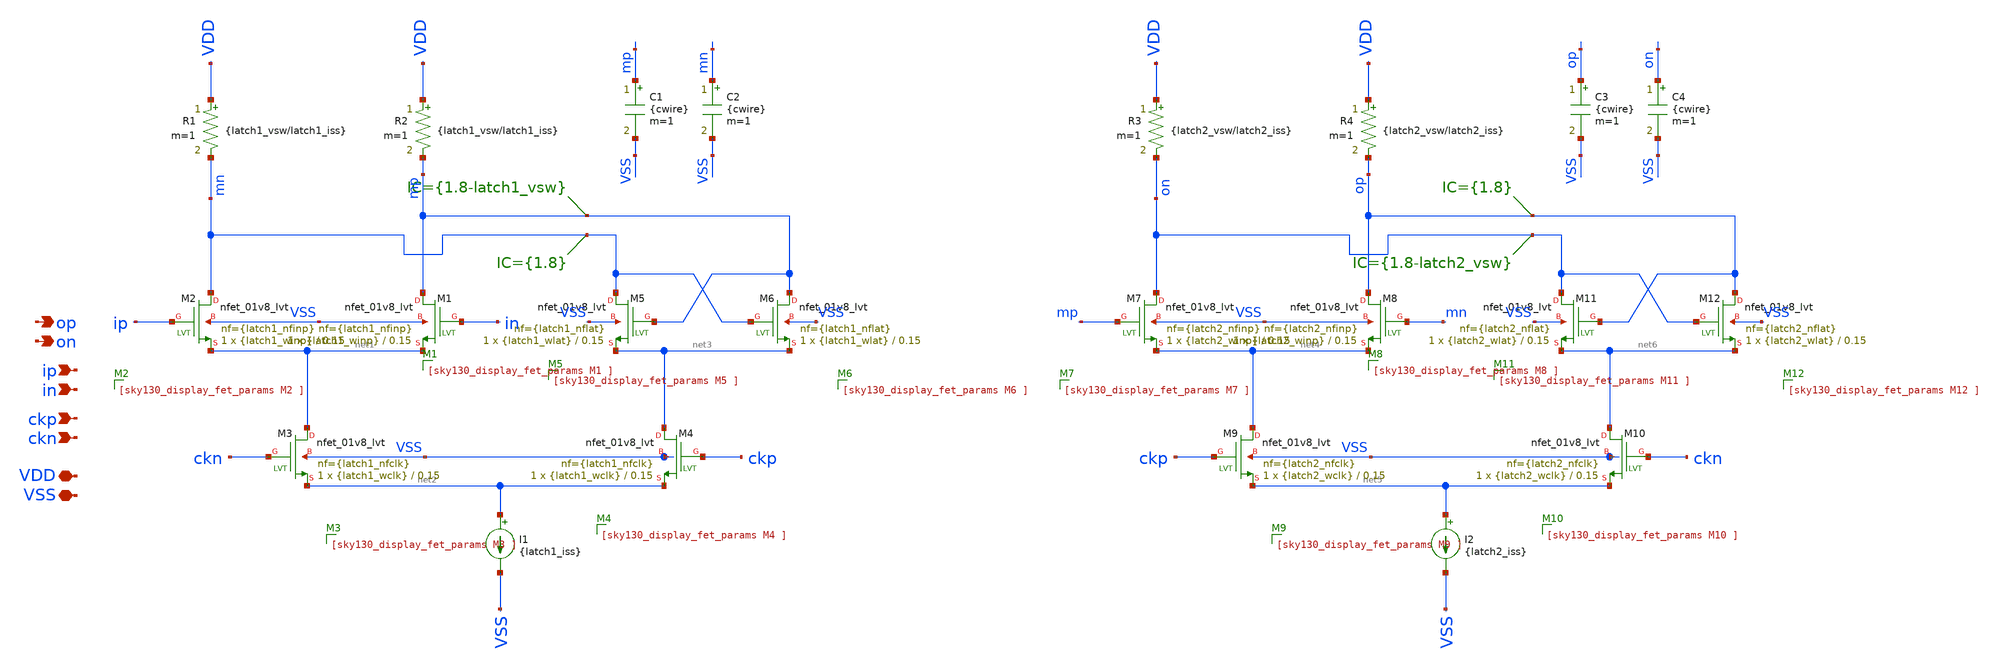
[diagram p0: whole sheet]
** sch_path: schematics/divider23/dff.sch
**.subckt dff VSS VDD op on ip in ckp ckn
*.iopin VSS
*.iopin VDD
*.opin op
*.opin on
*.ipin ip
*.ipin in
*.ipin ckp
*.ipin ckn
XM2 mn ip net1 VSS sky130_fd_pr__nfet_01v8_lvt L=0.15 W={latch1_winp} nf={latch1_nfinp} ad='int(({latch1_nfinp} + 1)/2) * {latch1_winp} / {latch1_nfinp} * 0.29'
+ as='int(({latch1_nfinp} + 2)/2) * {latch1_winp} / {latch1_nfinp} * 0.29' pd='2*int(({latch1_nfinp} + 1)/2) * ({latch1_winp} / {latch1_nfinp} + 0.29)'
+ ps='2*int(({latch1_nfinp} + 2)/2) * ({latch1_winp} / {latch1_nfinp} + 0.29)' nrd='0.29 / {latch1_winp} '
+ nrs='0.29 / {latch1_winp} ' sa=0 sb=0 sd=0 mult=1 m=1
XM1 mp in net1 VSS sky130_fd_pr__nfet_01v8_lvt L=0.15 W={latch1_winp} nf={latch1_nfinp} ad='int(({latch1_nfinp} + 1)/2) * {latch1_winp} / {latch1_nfinp} * 0.29'
+ as='int(({latch1_nfinp} + 2)/2) * {latch1_winp} / {latch1_nfinp} * 0.29' pd='2*int(({latch1_nfinp} + 1)/2) * ({latch1_winp} / {latch1_nfinp} + 0.29)'
+ ps='2*int(({latch1_nfinp} + 2)/2) * ({latch1_winp} / {latch1_nfinp} + 0.29)' nrd='0.29 / {latch1_winp} '
+ nrs='0.29 / {latch1_winp} ' sa=0 sb=0 sd=0 mult=1 m=1
I1 net2 VSS {latch1_iss}
XM3 net1 ckn net2 VSS sky130_fd_pr__nfet_01v8_lvt L=0.15 W={latch1_wclk} nf={latch1_nfclk} ad='int(({latch1_nfclk} + 1)/2) * {latch1_wclk} / {latch1_nfclk} * 0.29'
+ as='int(({latch1_nfclk} + 2)/2) * {latch1_wclk} / {latch1_nfclk} * 0.29' pd='2*int(({latch1_nfclk} + 1)/2) * ({latch1_wclk} / {latch1_nfclk} + 0.29)'
+ ps='2*int(({latch1_nfclk} + 2)/2) * ({latch1_wclk} / {latch1_nfclk} + 0.29)' nrd='0.29 / {latch1_wclk} '
+ nrs='0.29 / {latch1_wclk} ' sa=0 sb=0 sd=0 mult=1 m=1
XM4 net3 ckp net2 VSS sky130_fd_pr__nfet_01v8_lvt L=0.15 W={latch1_wclk} nf={latch1_nfclk} ad='int(({latch1_nfclk} + 1)/2) * {latch1_wclk} / {latch1_nfclk} * 0.29'
+ as='int(({latch1_nfclk} + 2)/2) * {latch1_wclk} / {latch1_nfclk} * 0.29' pd='2*int(({latch1_nfclk} + 1)/2) * ({latch1_wclk} / {latch1_nfclk} + 0.29)'
+ ps='2*int(({latch1_nfclk} + 2)/2) * ({latch1_wclk} / {latch1_nfclk} + 0.29)' nrd='0.29 / {latch1_wclk} '
+ nrs='0.29 / {latch1_wclk} ' sa=0 sb=0 sd=0 mult=1 m=1
XM5 mn mp net3 VSS sky130_fd_pr__nfet_01v8_lvt L=0.15 W={latch1_wlat} nf={latch1_nflat} ad='int(({latch1_nflat} + 1)/2) * {latch1_wlat} / {latch1_nflat} * 0.29'
+ as='int(({latch1_nflat} + 2)/2) * {latch1_wlat} / {latch1_nflat} * 0.29' pd='2*int(({latch1_nflat} + 1)/2) * ({latch1_wlat} / {latch1_nflat} + 0.29)'
+ ps='2*int(({latch1_nflat} + 2)/2) * ({latch1_wlat} / {latch1_nflat} + 0.29)' nrd='0.29 / {latch1_wlat} '
+ nrs='0.29 / {latch1_wlat} ' sa=0 sb=0 sd=0 mult=1 m=1
XM6 mp mn net3 VSS sky130_fd_pr__nfet_01v8_lvt L=0.15 W={latch1_wlat} nf={latch1_nflat} ad='int(({latch1_nflat} + 1)/2) * {latch1_wlat} / {latch1_nflat} * 0.29'
+ as='int(({latch1_nflat} + 2)/2) * {latch1_wlat} / {latch1_nflat} * 0.29' pd='2*int(({latch1_nflat} + 1)/2) * ({latch1_wlat} / {latch1_nflat} + 0.29)'
+ ps='2*int(({latch1_nflat} + 2)/2) * ({latch1_wlat} / {latch1_nflat} + 0.29)' nrd='0.29 / {latch1_wlat} '
+ nrs='0.29 / {latch1_wlat} ' sa=0 sb=0 sd=0 mult=1 m=1
C1 mp VSS {cwire} m=1
C2 mn VSS {cwire} m=1
.IC V(mp)={1.8-latch1_vsw}
.IC V(mn)={1.8}
XM7 on mp net4 VSS sky130_fd_pr__nfet_01v8_lvt L=0.15 W={latch2_winp} nf={latch2_nfinp} ad='int(({latch2_nfinp} + 1)/2) * {latch2_winp} / {latch2_nfinp} * 0.29'
+ as='int(({latch2_nfinp} + 2)/2) * {latch2_winp} / {latch2_nfinp} * 0.29' pd='2*int(({latch2_nfinp} + 1)/2) * ({latch2_winp} / {latch2_nfinp} + 0.29)'
+ ps='2*int(({latch2_nfinp} + 2)/2) * ({latch2_winp} / {latch2_nfinp} + 0.29)' nrd='0.29 / {latch2_winp} '
+ nrs='0.29 / {latch2_winp} ' sa=0 sb=0 sd=0 mult=1 m=1
XM8 op mn net4 VSS sky130_fd_pr__nfet_01v8_lvt L=0.15 W={latch2_winp} nf={latch2_nfinp} ad='int(({latch2_nfinp} + 1)/2) * {latch2_winp} / {latch2_nfinp} * 0.29'
+ as='int(({latch2_nfinp} + 2)/2) * {latch2_winp} / {latch2_nfinp} * 0.29' pd='2*int(({latch2_nfinp} + 1)/2) * ({latch2_winp} / {latch2_nfinp} + 0.29)'
+ ps='2*int(({latch2_nfinp} + 2)/2) * ({latch2_winp} / {latch2_nfinp} + 0.29)' nrd='0.29 / {latch2_winp} '
+ nrs='0.29 / {latch2_winp} ' sa=0 sb=0 sd=0 mult=1 m=1
I2 net5 VSS {latch2_iss}
XM9 net4 ckp net5 VSS sky130_fd_pr__nfet_01v8_lvt L=0.15 W={latch2_wclk} nf={latch2_nfclk} ad='int(({latch2_nfclk} + 1)/2) * {latch2_wclk} / {latch2_nfclk} * 0.29'
+ as='int(({latch2_nfclk} + 2)/2) * {latch2_wclk} / {latch2_nfclk} * 0.29' pd='2*int(({latch2_nfclk} + 1)/2) * ({latch2_wclk} / {latch2_nfclk} + 0.29)'
+ ps='2*int(({latch2_nfclk} + 2)/2) * ({latch2_wclk} / {latch2_nfclk} + 0.29)' nrd='0.29 / {latch2_wclk} '
+ nrs='0.29 / {latch2_wclk} ' sa=0 sb=0 sd=0 mult=1 m=1
XM10 net6 ckn net5 VSS sky130_fd_pr__nfet_01v8_lvt L=0.15 W={latch2_wclk} nf={latch2_nfclk} ad='int(({latch2_nfclk} + 1)/2) * {latch2_wclk} / {latch2_nfclk} * 0.29'
+ as='int(({latch2_nfclk} + 2)/2) * {latch2_wclk} / {latch2_nfclk} * 0.29' pd='2*int(({latch2_nfclk} + 1)/2) * ({latch2_wclk} / {latch2_nfclk} + 0.29)'
+ ps='2*int(({latch2_nfclk} + 2)/2) * ({latch2_wclk} / {latch2_nfclk} + 0.29)' nrd='0.29 / {latch2_wclk} '
+ nrs='0.29 / {latch2_wclk} ' sa=0 sb=0 sd=0 mult=1 m=1
XM11 on op net6 VSS sky130_fd_pr__nfet_01v8_lvt L=0.15 W={latch2_wlat} nf={latch2_nflat} ad='int(({latch2_nflat} + 1)/2) * {latch2_wlat} / {latch2_nflat} * 0.29'
+ as='int(({latch2_nflat} + 2)/2) * {latch2_wlat} / {latch2_nflat} * 0.29' pd='2*int(({latch2_nflat} + 1)/2) * ({latch2_wlat} / {latch2_nflat} + 0.29)'
+ ps='2*int(({latch2_nflat} + 2)/2) * ({latch2_wlat} / {latch2_nflat} + 0.29)' nrd='0.29 / {latch2_wlat} '
+ nrs='0.29 / {latch2_wlat} ' sa=0 sb=0 sd=0 mult=1 m=1
XM12 op on net6 VSS sky130_fd_pr__nfet_01v8_lvt L=0.15 W={latch2_wlat} nf={latch2_nflat} ad='int(({latch2_nflat} + 1)/2) * {latch2_wlat} / {latch2_nflat} * 0.29'
+ as='int(({latch2_nflat} + 2)/2) * {latch2_wlat} / {latch2_nflat} * 0.29' pd='2*int(({latch2_nflat} + 1)/2) * ({latch2_wlat} / {latch2_nflat} + 0.29)'
+ ps='2*int(({latch2_nflat} + 2)/2) * ({latch2_wlat} / {latch2_nflat} + 0.29)' nrd='0.29 / {latch2_wlat} '
+ nrs='0.29 / {latch2_wlat} ' sa=0 sb=0 sd=0 mult=1 m=1
C3 op VSS {cwire} m=1
C4 on VSS {cwire} m=1
.IC V(op)={1.8}
.IC V(on)={1.8-latch2_vsw}
R1 VDD mn {latch1_vsw/latch1_iss} m=1
R2 VDD mp {latch1_vsw/latch1_iss} m=1
R3 VDD on {latch2_vsw/latch2_iss} m=1
R4 VDD op {latch2_vsw/latch2_iss} m=1
**.ends
.end
